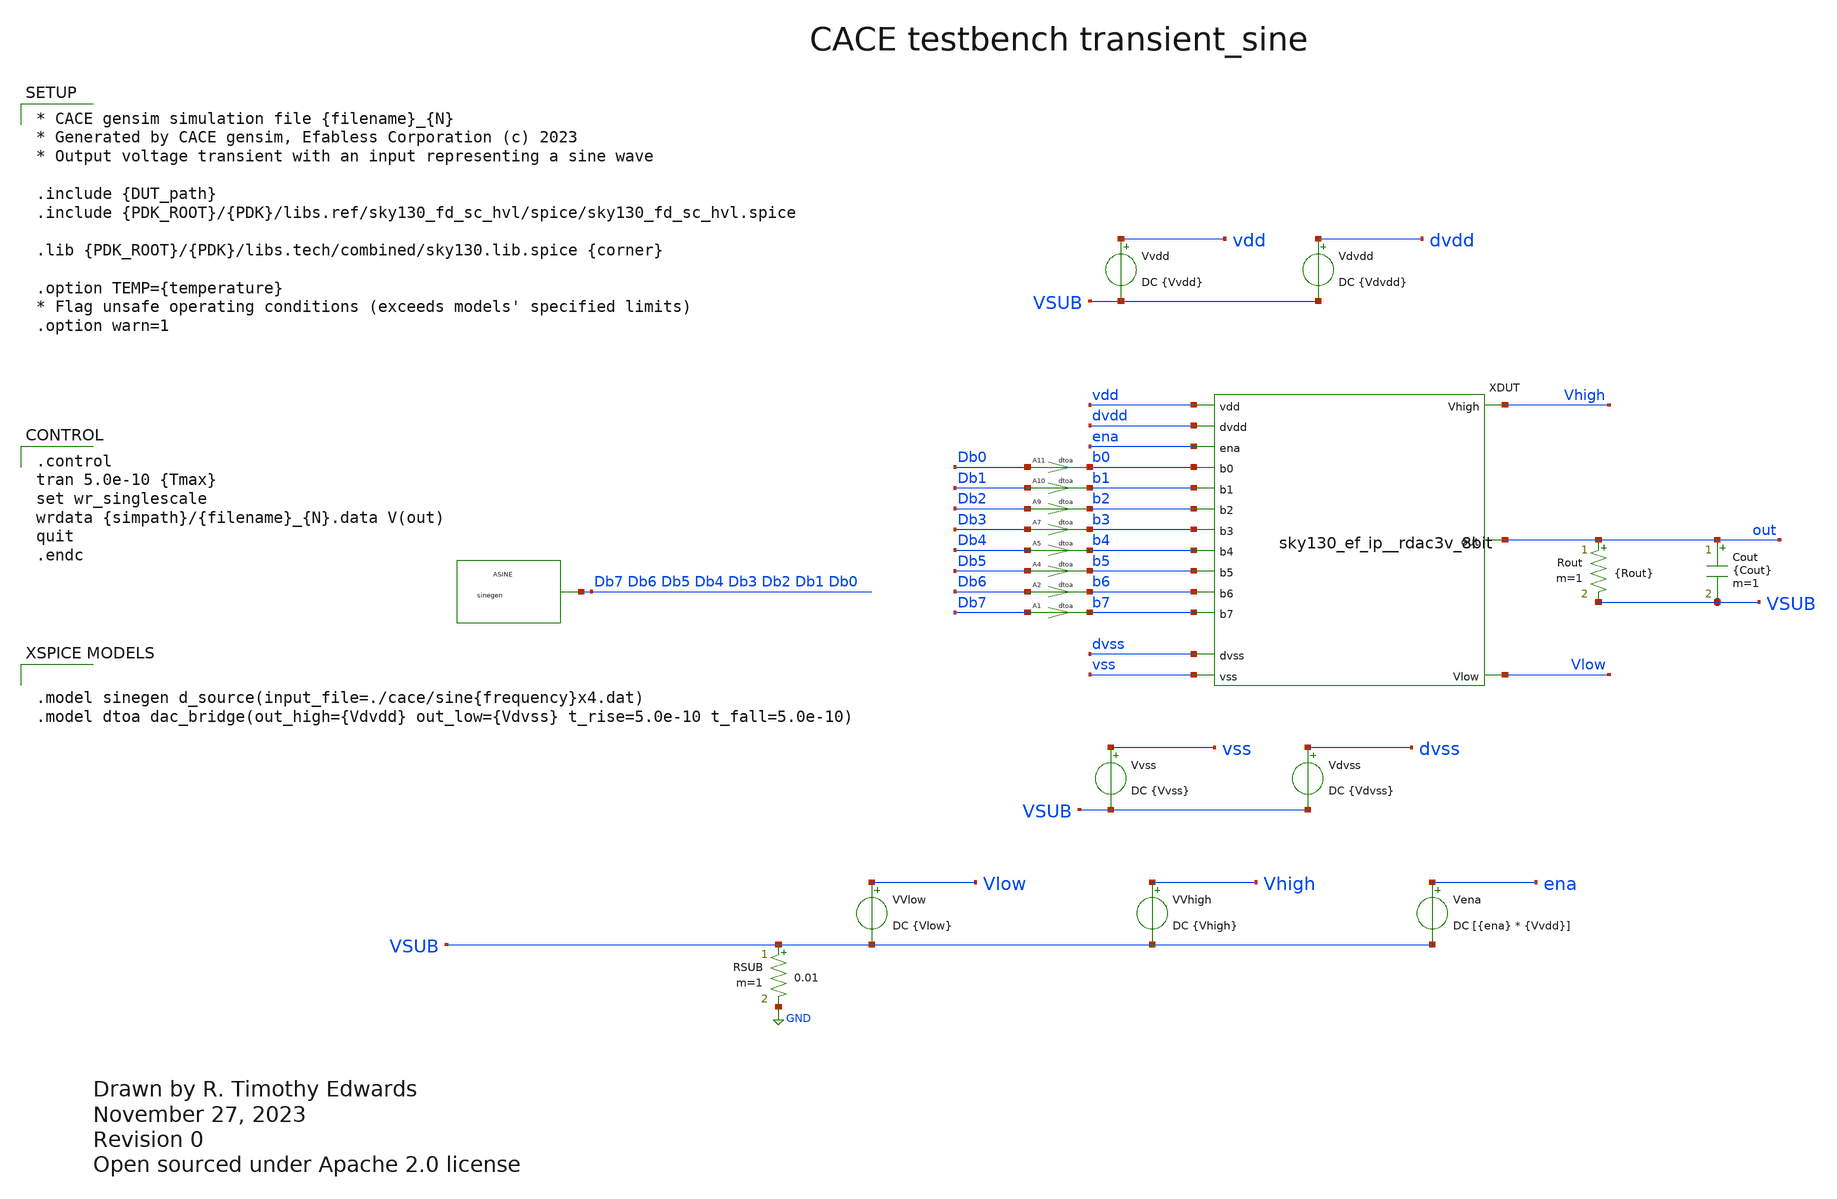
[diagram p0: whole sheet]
** sch_path: cace/transient_sine.sch
* Open sourced under Apache 2.0 license
**.subckt transient_sine
VVlow Vlow VSUB DC {Vlow}
VVhigh Vhigh VSUB DC {Vhigh}
Vena ena VSUB DC [{ena} * {Vvdd}]
Vvss vss VSUB DC {Vvss}
Rout out VSUB {Rout} m=1
Cout out VSUB {Cout} m=1
Vdvss dvss VSUB DC {Vdvss}
Vvdd vdd VSUB DC {Vvdd}
Vdvdd dvdd VSUB DC {Vdvdd}
RSUB VSUB GND 0.01 m=1
XDUT dvdd vss dvss vdd b0 Vhigh b1 b2 b3 out b4 b5 ena b6 b7 Vlow sky130_ef_ip__rdac3v_8bit
A1 [ Db7 ] [ b7 ] dtoa
A2 [ Db6 ] [ b6 ] dtoa
A4 [ Db5 ] [ b5 ] dtoa
A5 [ Db4 ] [ b4 ] dtoa
A7 [ Db3 ] [ b3 ] dtoa
A9 [ Db2 ] [ b2 ] dtoa
A10 [ Db1 ] [ b1 ] dtoa
A11 [ Db0 ] [ b0 ] dtoa
ASINE [ Db7 Db7 Db7 Db7 Db7 Db7 Db7 Db7 Db6 Db5 Db4 Db3 Db2 Db1 Db0 ] sinegen
**** begin user architecture code

.control
tran 5.0e-10 {Tmax}
set wr_singlescale
wrdata {simpath}/{filename}_{N}.data V(out)
quit
.endc



* CACE gensim simulation file {filename}_{N}
* Generated by CACE gensim, Efabless Corporation (c) 2023
* Output voltage transient with an input representing a sine wave

.include {DUT_path}
.include {PDK_ROOT}/{PDK}/libs.ref/sky130_fd_sc_hvl/spice/sky130_fd_sc_hvl.spice

.lib {PDK_ROOT}/{PDK}/libs.tech/combined/sky130.lib.spice {corner}

.option TEMP={temperature}
* Flag unsafe operating conditions (exceeds models' specified limits)
.option warn=1




.model sinegen d_source(input_file=./cace/sine{frequency}x4.dat)
.model dtoa dac_bridge(out_high={Vdvdd} out_low={Vdvss} t_rise=5.0e-10 t_fall=5.0e-10)


**** end user architecture code
**.ends
.GLOBAL GND
.end
